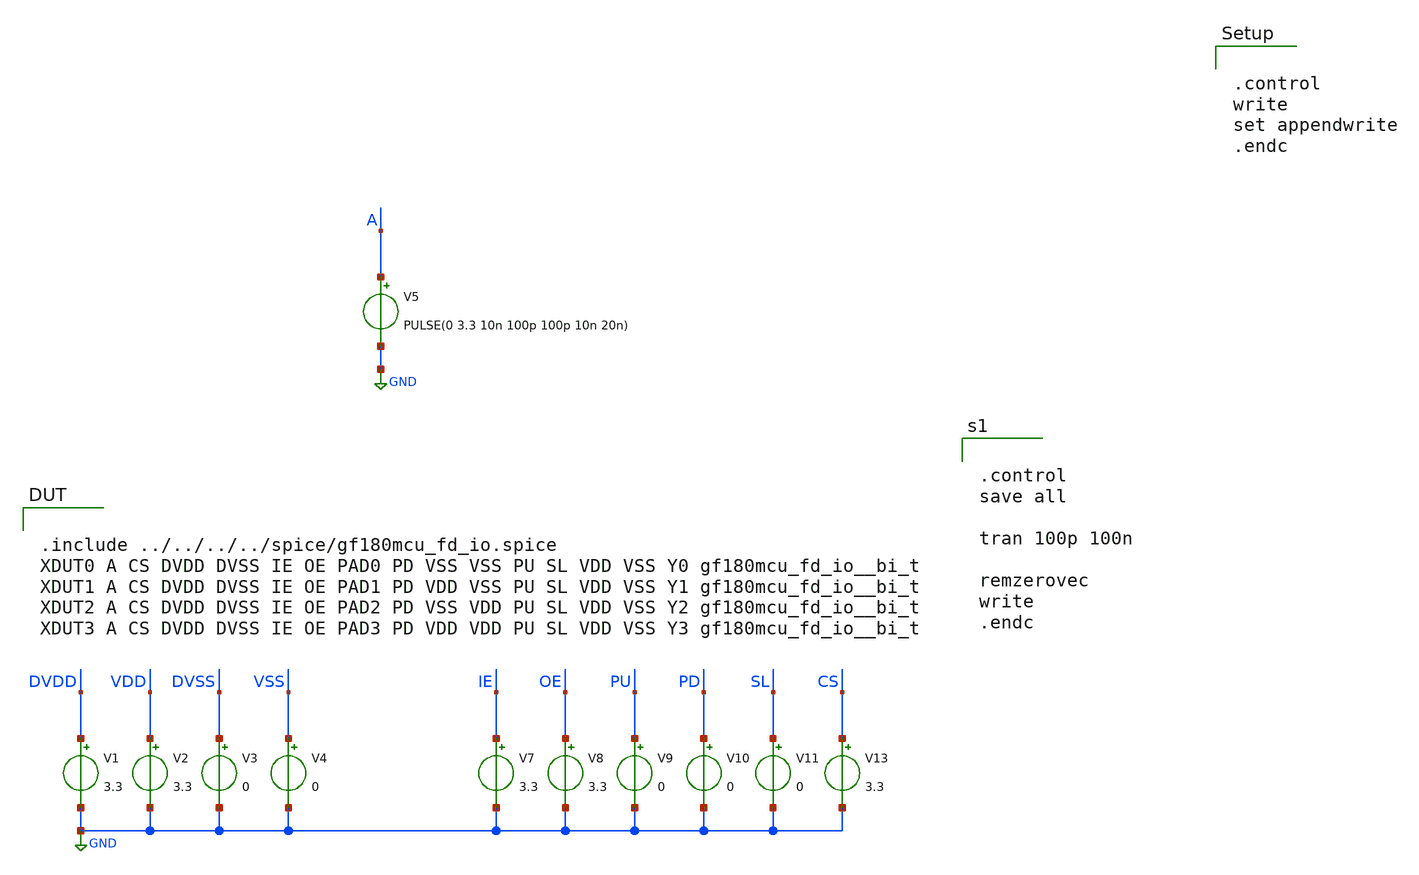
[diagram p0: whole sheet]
** sch_path: padframe/switching_bi_t/test/switching_bi_t.sch

.include $env(PDK_ROOT)/$env(PDK)/libs.tech/ngspice/design.ngspice
.lib $env(PDK_ROOT)/$env(PDK)/libs.tech/ngspice/sm141064.ngspice typical
.lib $env(PDK_ROOT)/$env(PDK)/libs.tech/ngspice/sm141064.ngspice diode_typical
.lib $env(PDK_ROOT)/$env(PDK)/libs.tech/ngspice/sm141064.ngspice res_typical
.lib $env(PDK_ROOT)/$env(PDK)/libs.tech/ngspice/sm141064.ngspice mimcap_typical
.lib $env(PDK_ROOT)/$env(PDK)/libs.tech/ngspice/sm141064.ngspice moscap_typical
.lib $env(PDK_ROOT)/$env(PDK)/libs.tech/ngspice/sm141064.ngspice bjt_typical
*.lib $env(PDK_ROOT)/$env(PDK)/libs.tech/ngspice/sm141064.ngspice cap_mim


.control
write
set appendwrite
.endc
**.subckt switching_bi_t
V1 DVDD GND 3.3
V2 VDD GND 3.3
V3 DVSS GND 0
V4 VSS GND 0
V5 A GND PULSE(0 3.3 10n 100p 100p 10n 20n)
V7 IE GND 3.3
V8 OE GND 3.3
V9 PU GND 0
V10 PD GND 0
V11 SL GND 0
V13 CS GND 3.3
**** begin user architecture code


.control
save all

tran 100p 100n

remzerovec
write
.endc



.include ../../../../spice/gf180mcu_fd_io.spice
XDUT0 A CS DVDD DVSS IE OE PAD0 PD VSS VSS PU SL VDD VSS Y0 gf180mcu_fd_io__bi_t
XDUT1 A CS DVDD DVSS IE OE PAD1 PD VDD VSS PU SL VDD VSS Y1 gf180mcu_fd_io__bi_t
XDUT2 A CS DVDD DVSS IE OE PAD2 PD VSS VDD PU SL VDD VSS Y2 gf180mcu_fd_io__bi_t
XDUT3 A CS DVDD DVSS IE OE PAD3 PD VDD VDD PU SL VDD VSS Y3 gf180mcu_fd_io__bi_t

**** end user architecture code
**.ends
.GLOBAL GND
.end
